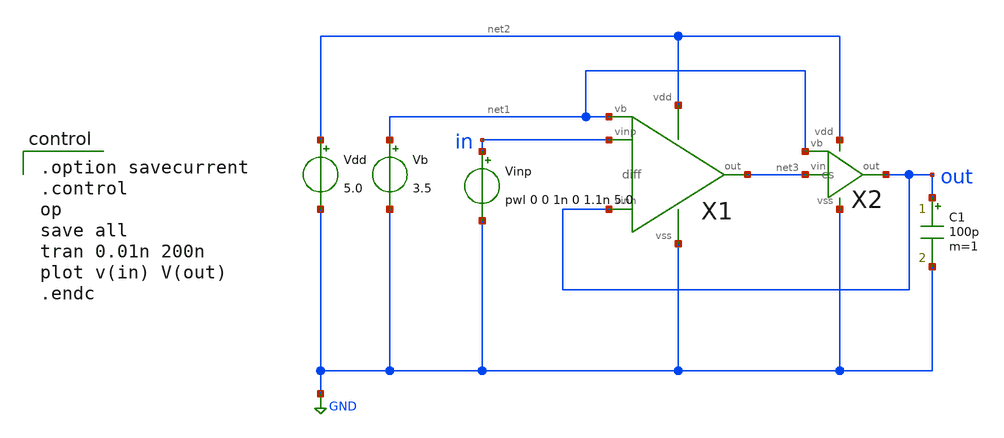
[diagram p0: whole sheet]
** sch_path: OpenSUSI-TR10/opamp/2stage_tran.sch
**.subckt 2stage_tran
Vdd net2 GND 5.0
Vb net1 GND 3.5
X1 in out net3 net2 GND net1 diff
X2 net3 net1 out net2 GND cs
C1 out GND 100p m=1
Vinp in GND pwl 0 0 1n 0 1.1n 5.0
**** begin user architecture code

.option savecurrent
.control
op
save all
tran 0.01n 200n
plot v(in) V(out)
.endc

 .include $::LIB/ip62_models
**** end user architecture code
**.ends

* expanding   symbol:  diff.sym # of pins=6
** sym_path: diff.sym
** sch_path: diff.sch
.subckt diff vinp vinn out vdd vss vb
*.ipin vinn
*.ipin vinp
*.ipin vb
*.opin out
*.iopin vdd
*.iopin vss
M5 net2 vb vdd vdd pmos L=2u W=40u m=1
M1 net1 vinn net2 net2 pmos L=2u W=200u m=1
M2 out vinp net2 net2 pmos L=2u W=200u m=1
M3 net1 net1 vss vss nmos L=2u W=10u m=1
M4 out net1 vss vss nmos L=2u W=10u m=1
.ends


* expanding   symbol:  cs.sym # of pins=5
** sym_path: cs.sym
** sch_path: cs.sch
.subckt cs vin vb out vdd vss
*.ipin vb
*.ipin vin
*.opin out
*.iopin vss
*.iopin vdd
XM6 out vb vdd vdd PMOS w=270u l=1u as=0 ad=0 ps=0 pd=0 nrd=0 nrs=0 m=1
XM7 out vin vss vss NMOS w=90u l=1u as=0 ad=0 ps=0 pd=0 nrd=0 nrs=0 m=1
.ends

.GLOBAL GND
.end
